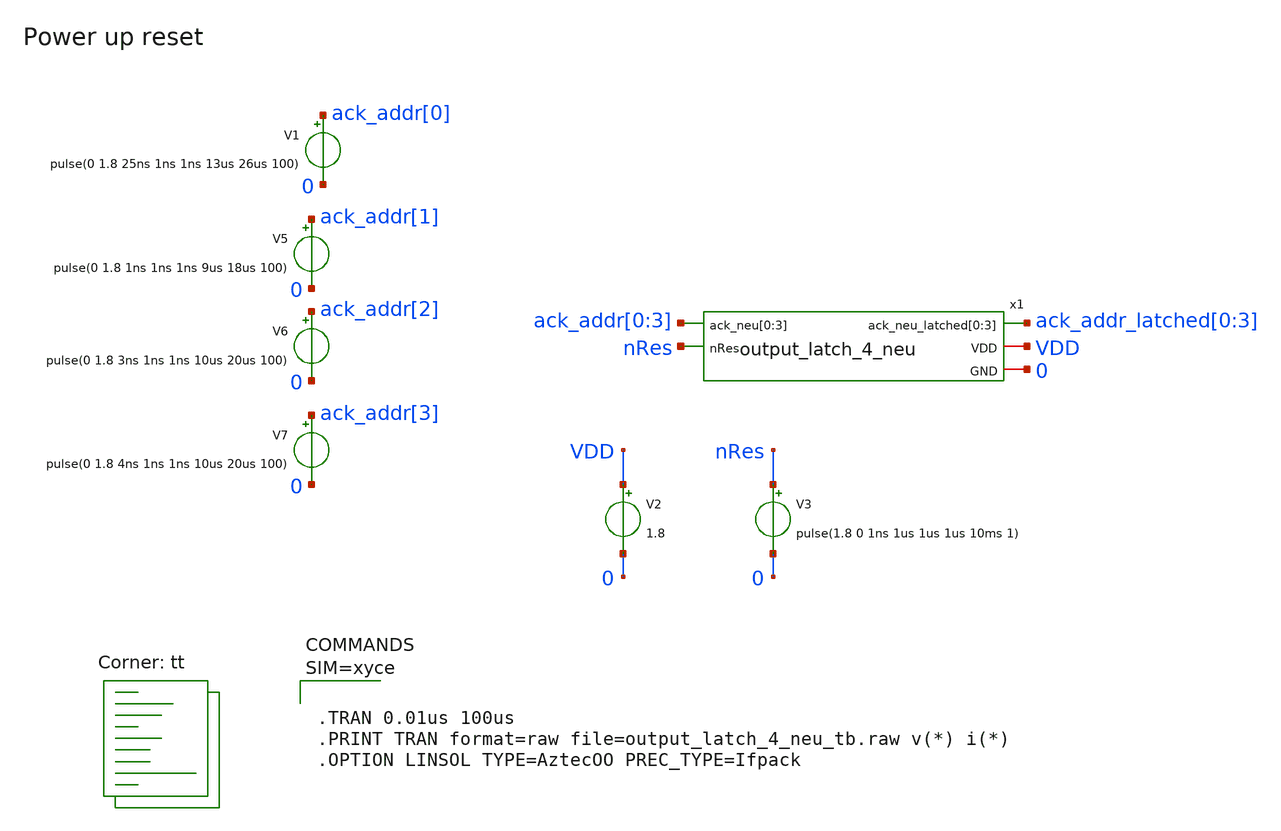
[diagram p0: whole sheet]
** sch_path: design/xschem/output_latch_4_neu_tb.sch
**.subckt output_latch_4_neu_tb
x1 ack_addr_latched[0] ack_addr_latched[1] ack_addr_latched[2] ack_addr_latched[3] ack_addr[0]
+ ack_addr[1] ack_addr[2] ack_addr[3] nRes VDD 0 output_latch_4_neu
V3 nRes 0 pulse(1.8 0 1ns 1us 1us 1us 10ms 1)
V1 ack_addr[0] 0 pulse(0 1.8 25ns 1ns 1ns 13us 26us 100)
V5 ack_addr[1] 0 pulse(0 1.8 1ns 1ns 1ns 9us 18us 100)
V6 ack_addr[2] 0 pulse(0 1.8 3ns 1ns 1ns 10us 20us 100)
V7 ack_addr[3] 0 pulse(0 1.8 4ns 1ns 1ns 10us 20us 100)
V2 VDD 0 1.8
**** begin user architecture code


* Standard cell simulation files
.include $::SKYWATER_STDCELLS/sky130_fd_sc_hd.spice


.lib $::SKYWATER_MODELS/sky130.lib.spice tt



**** end user architecture code
**.ends

* expanding   symbol:  output_latch_4_neu.sym # of pins=5
** sym_path: design/xschem/output_latch_4_neu.sym
** sch_path: design/xschem/output_latch_4_neu.sch
.subckt output_latch_4_neu ack_neu_latched[0] ack_neu_latched[1] ack_neu_latched[2]
+ ack_neu_latched[3] ack_neu[0] ack_neu[1] ack_neu[2] ack_neu[3] nRes VDD GND
*.ipin ack_neu[0],ack_neu[1],ack_neu[2],ack_neu[3]
*.ipin nRes
*.opin ack_neu_latched[0],ack_neu_latched[1],ack_neu_latched[2],ack_neu_latched[3]
*.iopin VDD
*.iopin GND
x2[0] latchAddr ack_neu[0] nRes GND GND VDD VDD ack_neu_latched[0] sky130_fd_sc_hd__dfrtp_1
x2[1] latchAddr ack_neu[1] nRes GND GND VDD VDD ack_neu_latched[1] sky130_fd_sc_hd__dfrtp_1
x2[2] latchAddr ack_neu[2] nRes GND GND VDD VDD ack_neu_latched[2] sky130_fd_sc_hd__dfrtp_1
x2[3] latchAddr ack_neu[3] nRes GND GND VDD VDD ack_neu_latched[3] sky130_fd_sc_hd__dfrtp_1
x6 ack_neu[0] ack_neu[1] GND GND VDD VDD net2 sky130_fd_sc_hd__or2_1
x1 ack_neu[2] ack_neu[3] GND GND VDD VDD net1 sky130_fd_sc_hd__or2_1
x2 net2 net1 GND GND VDD VDD latchAddr sky130_fd_sc_hd__or2_1
.ends

.end
